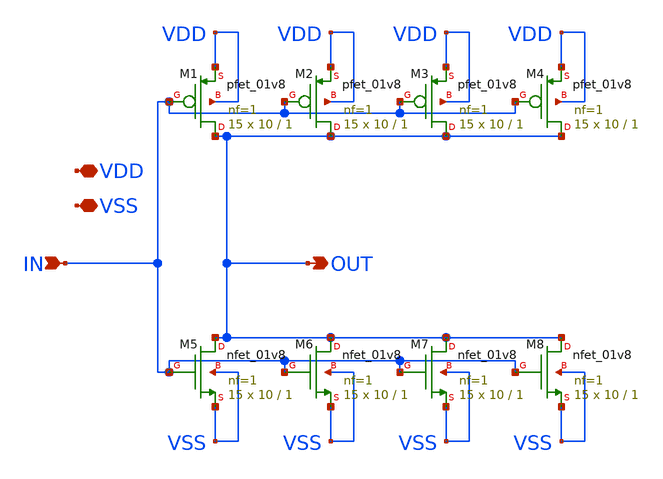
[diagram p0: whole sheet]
** sch_path: xschem/big_inverter.sch
**.subckt big_inverter VDD VSS IN OUT
*.iopin VDD
*.iopin VSS
*.ipin IN
*.opin OUT
XM1 OUT IN VDD VDD sky130_fd_pr__pfet_01v8 L=1 W=10 nf=1 ad='int((nf+1)/2) * W/nf * 0.29' as='int((nf+2)/2) * W/nf * 0.29'
+ pd='2*int((nf+1)/2) * (W/nf + 0.29)' ps='2*int((nf+2)/2) * (W/nf + 0.29)' nrd='0.29 / W' nrs='0.29 / W'
+ sa=0 sb=0 sd=0 mult=15 m=15
XM5 OUT IN VSS VSS sky130_fd_pr__nfet_01v8 L=1 W=10 nf=1 ad='int((nf+1)/2) * W/nf * 0.29' as='int((nf+2)/2) * W/nf * 0.29'
+ pd='2*int((nf+1)/2) * (W/nf + 0.29)' ps='2*int((nf+2)/2) * (W/nf + 0.29)' nrd='0.29 / W' nrs='0.29 / W'
+ sa=0 sb=0 sd=0 mult=15 m=15
XM2 OUT IN VDD VDD sky130_fd_pr__pfet_01v8 L=1 W=10 nf=1 ad='int((nf+1)/2) * W/nf * 0.29' as='int((nf+2)/2) * W/nf * 0.29'
+ pd='2*int((nf+1)/2) * (W/nf + 0.29)' ps='2*int((nf+2)/2) * (W/nf + 0.29)' nrd='0.29 / W' nrs='0.29 / W'
+ sa=0 sb=0 sd=0 mult=15 m=15
XM3 OUT IN VDD VDD sky130_fd_pr__pfet_01v8 L=1 W=10 nf=1 ad='int((nf+1)/2) * W/nf * 0.29' as='int((nf+2)/2) * W/nf * 0.29'
+ pd='2*int((nf+1)/2) * (W/nf + 0.29)' ps='2*int((nf+2)/2) * (W/nf + 0.29)' nrd='0.29 / W' nrs='0.29 / W'
+ sa=0 sb=0 sd=0 mult=15 m=15
XM4 OUT IN VDD VDD sky130_fd_pr__pfet_01v8 L=1 W=10 nf=1 ad='int((nf+1)/2) * W/nf * 0.29' as='int((nf+2)/2) * W/nf * 0.29'
+ pd='2*int((nf+1)/2) * (W/nf + 0.29)' ps='2*int((nf+2)/2) * (W/nf + 0.29)' nrd='0.29 / W' nrs='0.29 / W'
+ sa=0 sb=0 sd=0 mult=15 m=15
XM6 OUT IN VSS VSS sky130_fd_pr__nfet_01v8 L=1 W=10 nf=1 ad='int((nf+1)/2) * W/nf * 0.29' as='int((nf+2)/2) * W/nf * 0.29'
+ pd='2*int((nf+1)/2) * (W/nf + 0.29)' ps='2*int((nf+2)/2) * (W/nf + 0.29)' nrd='0.29 / W' nrs='0.29 / W'
+ sa=0 sb=0 sd=0 mult=15 m=15
XM7 OUT IN VSS VSS sky130_fd_pr__nfet_01v8 L=1 W=10 nf=1 ad='int((nf+1)/2) * W/nf * 0.29' as='int((nf+2)/2) * W/nf * 0.29'
+ pd='2*int((nf+1)/2) * (W/nf + 0.29)' ps='2*int((nf+2)/2) * (W/nf + 0.29)' nrd='0.29 / W' nrs='0.29 / W'
+ sa=0 sb=0 sd=0 mult=15 m=15
XM8 OUT IN VSS VSS sky130_fd_pr__nfet_01v8 L=1 W=10 nf=1 ad='int((nf+1)/2) * W/nf * 0.29' as='int((nf+2)/2) * W/nf * 0.29'
+ pd='2*int((nf+1)/2) * (W/nf + 0.29)' ps='2*int((nf+2)/2) * (W/nf + 0.29)' nrd='0.29 / W' nrs='0.29 / W'
+ sa=0 sb=0 sd=0 mult=15 m=15
**.ends
.end
